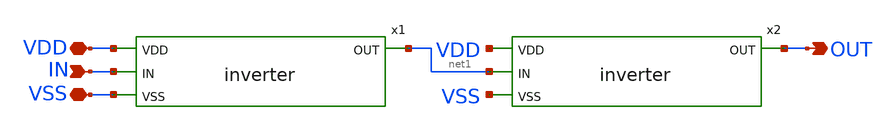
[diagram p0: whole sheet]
** sch_path: xschem/buffer.sch
**.subckt buffer VSS VDD IN OUT
*.iopin VSS
*.iopin VDD
*.ipin IN
*.opin OUT
x1 VDD IN net1 VSS inverter
x2 VDD net1 OUT VSS inverter
**.ends
.end
